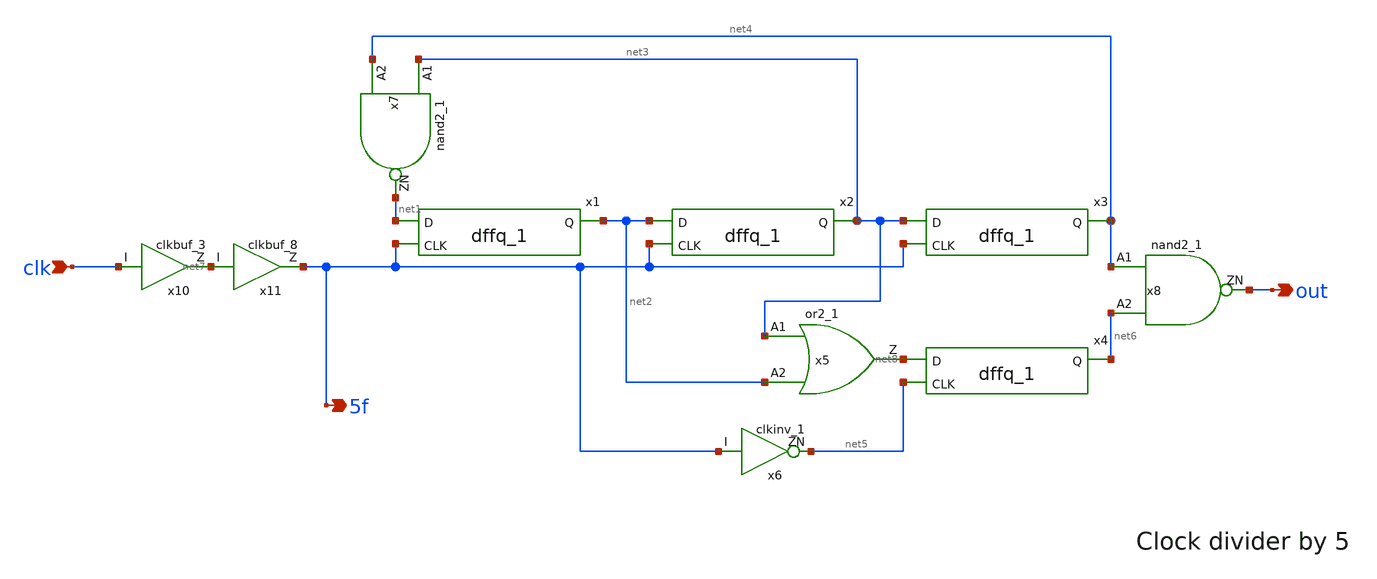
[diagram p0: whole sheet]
** sch_path: PLL/xschem/fdiv.sch
**.subckt fdiv clk out 5f
*.ipin clk
*.opin out
*.opin 5f
x10 clk net7 VDD VDD 0 0 gf180mcu_fd_sc_mcu7t5v0__clkbuf_3
x11 net7 5f VDD VDD 0 0 gf180mcu_fd_sc_mcu7t5v0__clkbuf_8
x1 net1 5f net2 VDD VDD 0 0 gf180mcu_fd_sc_mcu7t5v0__dffq_1
x7 net3 net4 net1 VDD VDD 0 0 gf180mcu_fd_sc_mcu7t5v0__nand2_1
x2 net2 5f net3 VDD VDD 0 0 gf180mcu_fd_sc_mcu7t5v0__dffq_1
x3 net3 5f net4 VDD VDD 0 0 gf180mcu_fd_sc_mcu7t5v0__dffq_1
x4 net8 net5 net6 VDD VDD 0 0 gf180mcu_fd_sc_mcu7t5v0__dffq_1
x5 net3 net2 net8 VDD VDD 0 0 gf180mcu_fd_sc_mcu7t5v0__or2_1
x6 5f net5 VDD VDD 0 0 gf180mcu_fd_sc_mcu7t5v0__clkinv_1
x8 net4 net6 out VDD VDD 0 0 gf180mcu_fd_sc_mcu7t5v0__nand2_1
**.ends
.end
